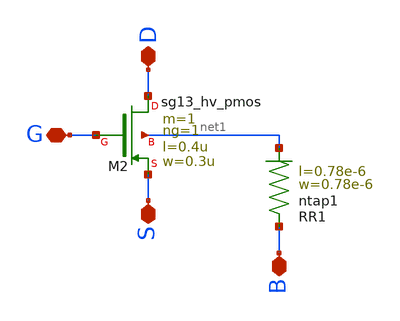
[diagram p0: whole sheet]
** sch_path: ihp-sg13cmos5l/schematic/xschem/sg13_hv_pmos_tap.sch
**.subckt sg13_hv_pmos_tap D S G B
*.iopin D
*.iopin S
*.iopin G
*.iopin B
XR1 B net1 ntap1 R=262.8 w=0.78e-6 l=0.78e-6
XM2 D G S net1 sg13_hv_pmos w=0.3u l=0.4u ng=1 m=1 mm_ok=1
**.ends
.end
